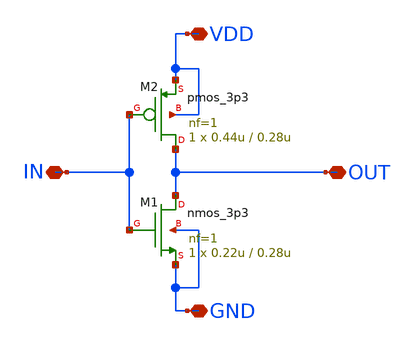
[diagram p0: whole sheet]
** sch_path: ipdesignguide/tutorial/inverter/inverter.sch
**.subckt inverter OUT VDD GND IN
*.iopin OUT
*.iopin VDD
*.iopin GND
*.iopin IN
XM1 OUT IN GND GND nmos_3p3 L=0.28u W=0.22u nf=1 ad='int((nf+1)/2) * W/nf * 0.18u' as='int((nf+2)/2) * W/nf * 0.18u'
+ pd='2*int((nf+1)/2) * (W/nf + 0.18u)' ps='2*int((nf+2)/2) * (W/nf + 0.18u)' nrd='0.18u / W' nrs='0.18u / W'
+ sa=0 sb=0 sd=0 m=1
XM2 OUT IN VDD VDD pmos_3p3 L=0.28u W=0.44u nf=1 ad='int((nf+1)/2) * W/nf * 0.18u' as='int((nf+2)/2) * W/nf * 0.18u'
+ pd='2*int((nf+1)/2) * (W/nf + 0.18u)' ps='2*int((nf+2)/2) * (W/nf + 0.18u)' nrd='0.18u / W' nrs='0.18u / W'
+ sa=0 sb=0 sd=0 m=1
**.ends
.end
